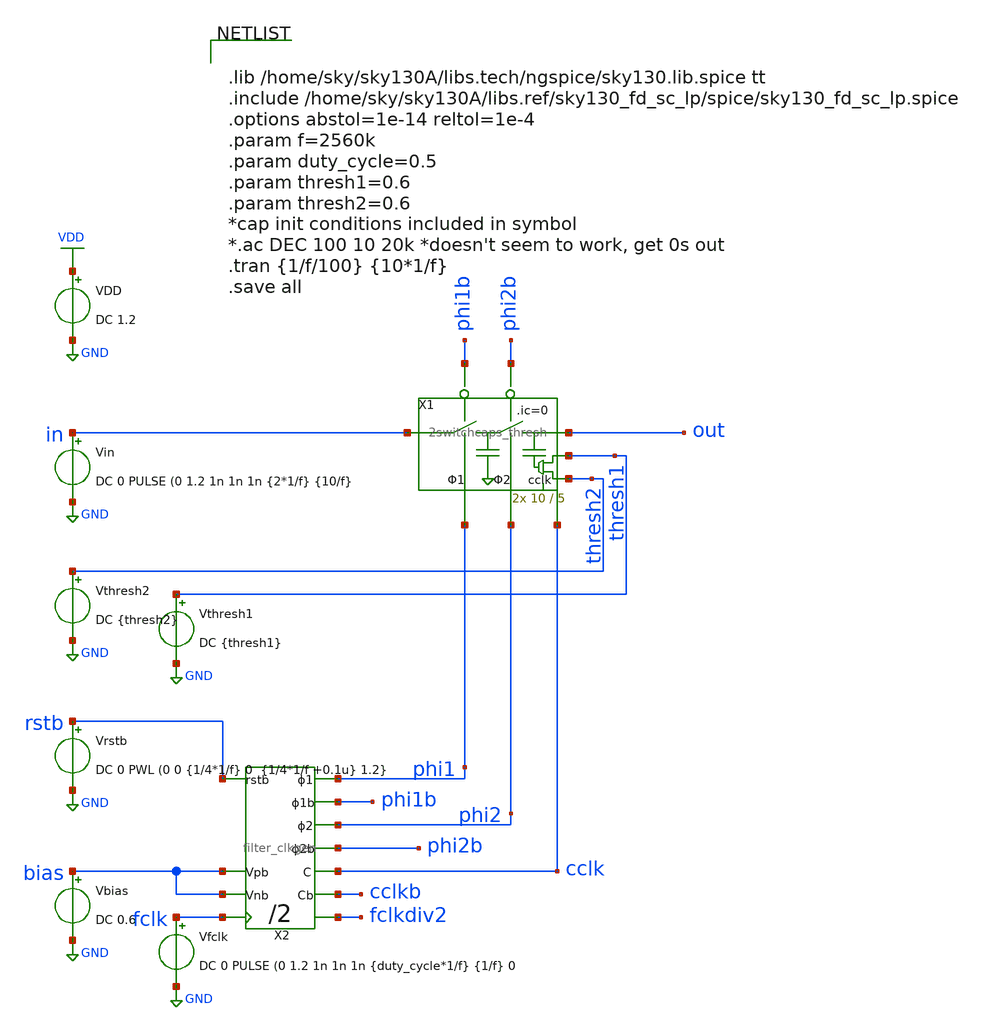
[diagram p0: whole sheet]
** sch_path: xschem/Switched_Caps/2switchcaps_thresh_tb.sch
**.subckt 2switchcaps_thresh_tb
Vin in GND DC 0 PULSE (0 1.2 1n 1n 1n {2*1/f} {10/f}
VDD VDD GND DC 1.2
Vfclk fclk GND DC 0 PULSE (0 1.2 1n 1n 1n {duty_cycle*1/f} {1/f} 0
X1 in out phi2 phi1 phi1b phi2b thresh2 cclk thresh1 2switchcaps_thresh Wcap=10 Lcap=5
X2 rstb fclk phi2b phi2 phi1b phi1 cclkb cclk fclkdiv2 bias bias filter_clkgen
Vbias bias GND DC 0.6
Vthresh1 thresh1 GND DC {thresh1}
Vthresh2 thresh2 GND DC {thresh2}
Vrstb rstb GND DC 0 PWL (0 0 {1/4*1/f} 0 {1/4*1/f +0.1u} 1.2}
**** begin user architecture code


.lib /home/sky/sky130A/libs.tech/ngspice/sky130.lib.spice tt
.include /home/sky/sky130A/libs.ref/sky130_fd_sc_lp/spice/sky130_fd_sc_lp.spice
.options abstol=1e-14 reltol=1e-4
.param f=2560k
.param duty_cycle=0.5
.param thresh1=0.6
.param thresh2=0.6
*cap init conditions included in symbol
*.ac DEC 100 10 20k *doesn't seem to work, get 0s out
.tran {1/f/100} {10*1/f}
.save all


**** end user architecture code
**.ends
.GLOBAL GND
.GLOBAL VDD
.end
